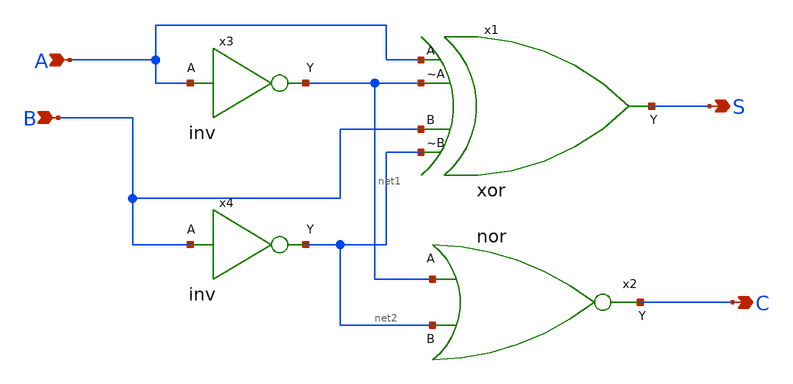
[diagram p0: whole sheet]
** sch_path: circuits/xschem/half_adder.sch
**.subckt half_adder A B S C
*.ipin A
*.ipin B
*.opin S
*.opin C
x1 B S A net1 net2 xor
x2 C net1 net2 nor
x3 net1 A inv
x4 net2 B inv
**.ends
.end
